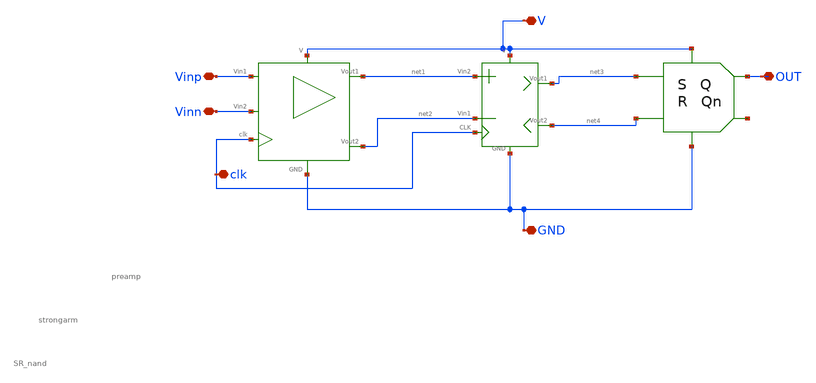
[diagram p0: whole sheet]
** sch_path: V2/Simbolos/Preamp-Strong-Latch.sch
**.subckt Preamp-Strong-Latch V GND Vinp Vinn clk OUT
*.iopin V
*.iopin GND
*.iopin Vinp
*.iopin Vinn
*.iopin clk
*.iopin OUT
X1 net3 V GND net4 OUT net5 SR_nand
X3 V GND Vinp clk net1 net2 Vinn preamp
X4 V GND net2 net1 clk net3 net4 strongarm
**.ends

* expanding   symbol:  jesusu/Simbolos/SR_nand.sym # of pins=6
** sym_path: Simbolos/SR_nand.sym
** sch_path: Simbolos/SR_nand.sch
.subckt SR_nand S V GND R Q Qn
*.iopin S
*.iopin R
*.iopin V
*.iopin GND
*.iopin Qn
*.iopin Q
XM1 Qn S V V pfet_03v3 L=0.28u W=4u nf=1 ad='int((nf+1)/2) * W/nf * 0.18u' as='int((nf+2)/2) * W/nf * 0.18u'
+ pd='2*int((nf+1)/2) * (W/nf + 0.18u)' ps='2*int((nf+2)/2) * (W/nf + 0.18u)' nrd='0.18u / W' nrs='0.18u / W'
+ sa=0 sb=0 sd=0 m=1
XM2 Qn Q net1 GND nfet_03v3 L=0.28u W=4u nf=1 ad='int((nf+1)/2) * W/nf * 0.18u' as='int((nf+2)/2) * W/nf * 0.18u'
+ pd='2*int((nf+1)/2) * (W/nf + 0.18u)' ps='2*int((nf+2)/2) * (W/nf + 0.18u)' nrd='0.18u / W' nrs='0.18u / W'
+ sa=0 sb=0 sd=0 m=1
XM3 Q Qn V V pfet_03v3 L=0.28u W=4u nf=1 ad='int((nf+1)/2) * W/nf * 0.18u' as='int((nf+2)/2) * W/nf * 0.18u'
+ pd='2*int((nf+1)/2) * (W/nf + 0.18u)' ps='2*int((nf+2)/2) * (W/nf + 0.18u)' nrd='0.18u / W' nrs='0.18u / W'
+ sa=0 sb=0 sd=0 m=1
XM4 Q R V V pfet_03v3 L=0.28u W=4u nf=1 ad='int((nf+1)/2) * W/nf * 0.18u' as='int((nf+2)/2) * W/nf * 0.18u'
+ pd='2*int((nf+1)/2) * (W/nf + 0.18u)' ps='2*int((nf+2)/2) * (W/nf + 0.18u)' nrd='0.18u / W' nrs='0.18u / W'
+ sa=0 sb=0 sd=0 m=1
XM5 Qn Q V V pfet_03v3 L=0.28u W=4u nf=1 ad='int((nf+1)/2) * W/nf * 0.18u' as='int((nf+2)/2) * W/nf * 0.18u'
+ pd='2*int((nf+1)/2) * (W/nf + 0.18u)' ps='2*int((nf+2)/2) * (W/nf + 0.18u)' nrd='0.18u / W' nrs='0.18u / W'
+ sa=0 sb=0 sd=0 m=1
XM6 net1 S GND GND nfet_03v3 L=0.28u W=4u nf=1 ad='int((nf+1)/2) * W/nf * 0.18u' as='int((nf+2)/2) * W/nf * 0.18u'
+ pd='2*int((nf+1)/2) * (W/nf + 0.18u)' ps='2*int((nf+2)/2) * (W/nf + 0.18u)' nrd='0.18u / W' nrs='0.18u / W'
+ sa=0 sb=0 sd=0 m=1
XM7 Q Qn net2 GND nfet_03v3 L=0.28u W=4u nf=1 ad='int((nf+1)/2) * W/nf * 0.18u' as='int((nf+2)/2) * W/nf * 0.18u'
+ pd='2*int((nf+1)/2) * (W/nf + 0.18u)' ps='2*int((nf+2)/2) * (W/nf + 0.18u)' nrd='0.18u / W' nrs='0.18u / W'
+ sa=0 sb=0 sd=0 m=1
XM8 net2 R GND GND nfet_03v3 L=0.28u W=2u nf=1 ad='int((nf+1)/2) * W/nf * 0.18u' as='int((nf+2)/2) * W/nf * 0.18u'
+ pd='2*int((nf+1)/2) * (W/nf + 0.18u)' ps='2*int((nf+2)/2) * (W/nf + 0.18u)' nrd='0.18u / W' nrs='0.18u / W'
+ sa=0 sb=0 sd=0 m=1
.ends


* expanding   symbol:  jesusu/Simbolos/preamp.sym # of pins=7
** sym_path: Simbolos/preamp.sym
** sch_path: Simbolos/preamp.sch
.subckt preamp V GND Vin1 clk Vout1 Vout2 Vin2
*.iopin V
*.iopin GND
*.iopin Vout2
*.iopin Vout1
*.iopin clk
*.iopin Vin2
*.iopin Vin1
XM26 Vout2 Vin1 net1 GND nfet_03v3 L=0.28u W=10u nf=1 ad='int((nf+1)/2) * W/nf * 0.18u' as='int((nf+2)/2) * W/nf * 0.18u'
+ pd='2*int((nf+1)/2) * (W/nf + 0.18u)' ps='2*int((nf+2)/2) * (W/nf + 0.18u)' nrd='0.18u / W' nrs='0.18u / W'
+ sa=0 sb=0 sd=0 m=1
XM27 Vout1 Vin2 net1 GND nfet_03v3 L=0.28u W=10u nf=1 ad='int((nf+1)/2) * W/nf * 0.18u' as='int((nf+2)/2) * W/nf * 0.18u'
+ pd='2*int((nf+1)/2) * (W/nf + 0.18u)' ps='2*int((nf+2)/2) * (W/nf + 0.18u)' nrd='0.18u / W' nrs='0.18u / W'
+ sa=0 sb=0 sd=0 m=1
XM28 net1 clk GND GND nfet_03v3 L=0.28u W=1u nf=1 ad='int((nf+1)/2) * W/nf * 0.18u' as='int((nf+2)/2) * W/nf * 0.18u'
+ pd='2*int((nf+1)/2) * (W/nf + 0.18u)' ps='2*int((nf+2)/2) * (W/nf + 0.18u)' nrd='0.18u / W' nrs='0.18u / W'
+ sa=0 sb=0 sd=0 m=1
XM24 Vout1 clk V V pfet_03v3 L=0.28u W=1u nf=1 ad='int((nf+1)/2) * W/nf * 0.18u' as='int((nf+2)/2) * W/nf * 0.18u'
+ pd='2*int((nf+1)/2) * (W/nf + 0.18u)' ps='2*int((nf+2)/2) * (W/nf + 0.18u)' nrd='0.18u / W' nrs='0.18u / W'
+ sa=0 sb=0 sd=0 m=1
XM25 Vout2 clk V V pfet_03v3 L=0.28u W=1u nf=1 ad='int((nf+1)/2) * W/nf * 0.18u' as='int((nf+2)/2) * W/nf * 0.18u'
+ pd='2*int((nf+1)/2) * (W/nf + 0.18u)' ps='2*int((nf+2)/2) * (W/nf + 0.18u)' nrd='0.18u / W' nrs='0.18u / W'
+ sa=0 sb=0 sd=0 m=1
C1 Vout1 GND 30f m=1
C2 Vout2 GND 30f m=1
.ends


* expanding   symbol:  jesusu/Simbolos/strongarm.sym # of pins=7
** sym_path: V2/Symbols/strongarm.sym
** sch_path: V2/Symbols/strongarm.sch
.subckt strongarm V GND Vin1 Vin2 CLK Vout1 Vout2
*.iopin V
*.iopin Vout1
*.iopin Vin1
*.iopin Vin2
*.iopin Vout2
*.iopin CLK
*.iopin GND
XM1 net2 Vout2 V V pfet_03v3 L=0.28u W=0.22u nf=1 ad='int((nf+1)/2) * W/nf * 0.18u' as='int((nf+2)/2) * W/nf * 0.18u'
+ pd='2*int((nf+1)/2) * (W/nf + 0.18u)' ps='2*int((nf+2)/2) * (W/nf + 0.18u)' nrd='0.18u / W' nrs='0.18u / W'
+ sa=0 sb=0 sd=0 m=1
XM2 Vout1 CLK GND GND nfet_03v3 L=0.28u W=0.22u nf=1 ad='int((nf+1)/2) * W/nf * 0.18u' as='int((nf+2)/2) * W/nf * 0.18u'
+ pd='2*int((nf+1)/2) * (W/nf + 0.18u)' ps='2*int((nf+2)/2) * (W/nf + 0.18u)' nrd='0.18u / W' nrs='0.18u / W'
+ sa=0 sb=0 sd=0 m=1
XM3 Vout2 Vout1 GND GND nfet_03v3 L=0.28u W=0.22u nf=1 ad='int((nf+1)/2) * W/nf * 0.18u' as='int((nf+2)/2) * W/nf * 0.18u'
+ pd='2*int((nf+1)/2) * (W/nf + 0.18u)' ps='2*int((nf+2)/2) * (W/nf + 0.18u)' nrd='0.18u / W' nrs='0.18u / W'
+ sa=0 sb=0 sd=0 m=1
XM4 Vout2 CLK GND GND nfet_03v3 L=0.28u W=0.22u nf=1 ad='int((nf+1)/2) * W/nf * 0.18u' as='int((nf+2)/2) * W/nf * 0.18u'
+ pd='2*int((nf+1)/2) * (W/nf + 0.18u)' ps='2*int((nf+2)/2) * (W/nf + 0.18u)' nrd='0.18u / W' nrs='0.18u / W'
+ sa=0 sb=0 sd=0 m=1
XM5 Vout1 Vout2 GND GND nfet_03v3 L=0.28u W=0.22u nf=1 ad='int((nf+1)/2) * W/nf * 0.18u' as='int((nf+2)/2) * W/nf * 0.18u'
+ pd='2*int((nf+1)/2) * (W/nf + 0.18u)' ps='2*int((nf+2)/2) * (W/nf + 0.18u)' nrd='0.18u / W' nrs='0.18u / W'
+ sa=0 sb=0 sd=0 m=1
XM6 net1 Vout1 V V pfet_03v3 L=0.28u W=0.22u nf=1 ad='int((nf+1)/2) * W/nf * 0.18u' as='int((nf+2)/2) * W/nf * 0.18u'
+ pd='2*int((nf+1)/2) * (W/nf + 0.18u)' ps='2*int((nf+2)/2) * (W/nf + 0.18u)' nrd='0.18u / W' nrs='0.18u / W'
+ sa=0 sb=0 sd=0 m=1
XM7 Vout1 Vin1 net2 V pfet_03v3 L=0.28u W=0.22u nf=1 ad='int((nf+1)/2) * W/nf * 0.18u' as='int((nf+2)/2) * W/nf * 0.18u'
+ pd='2*int((nf+1)/2) * (W/nf + 0.18u)' ps='2*int((nf+2)/2) * (W/nf + 0.18u)' nrd='0.18u / W' nrs='0.18u / W'
+ sa=0 sb=0 sd=0 m=1
XM8 Vout2 Vin2 net1 V pfet_03v3 L=0.28u W=0.22u nf=1 ad='int((nf+1)/2) * W/nf * 0.18u' as='int((nf+2)/2) * W/nf * 0.18u'
+ pd='2*int((nf+1)/2) * (W/nf + 0.18u)' ps='2*int((nf+2)/2) * (W/nf + 0.18u)' nrd='0.18u / W' nrs='0.18u / W'
+ sa=0 sb=0 sd=0 m=1
.ends

.end
